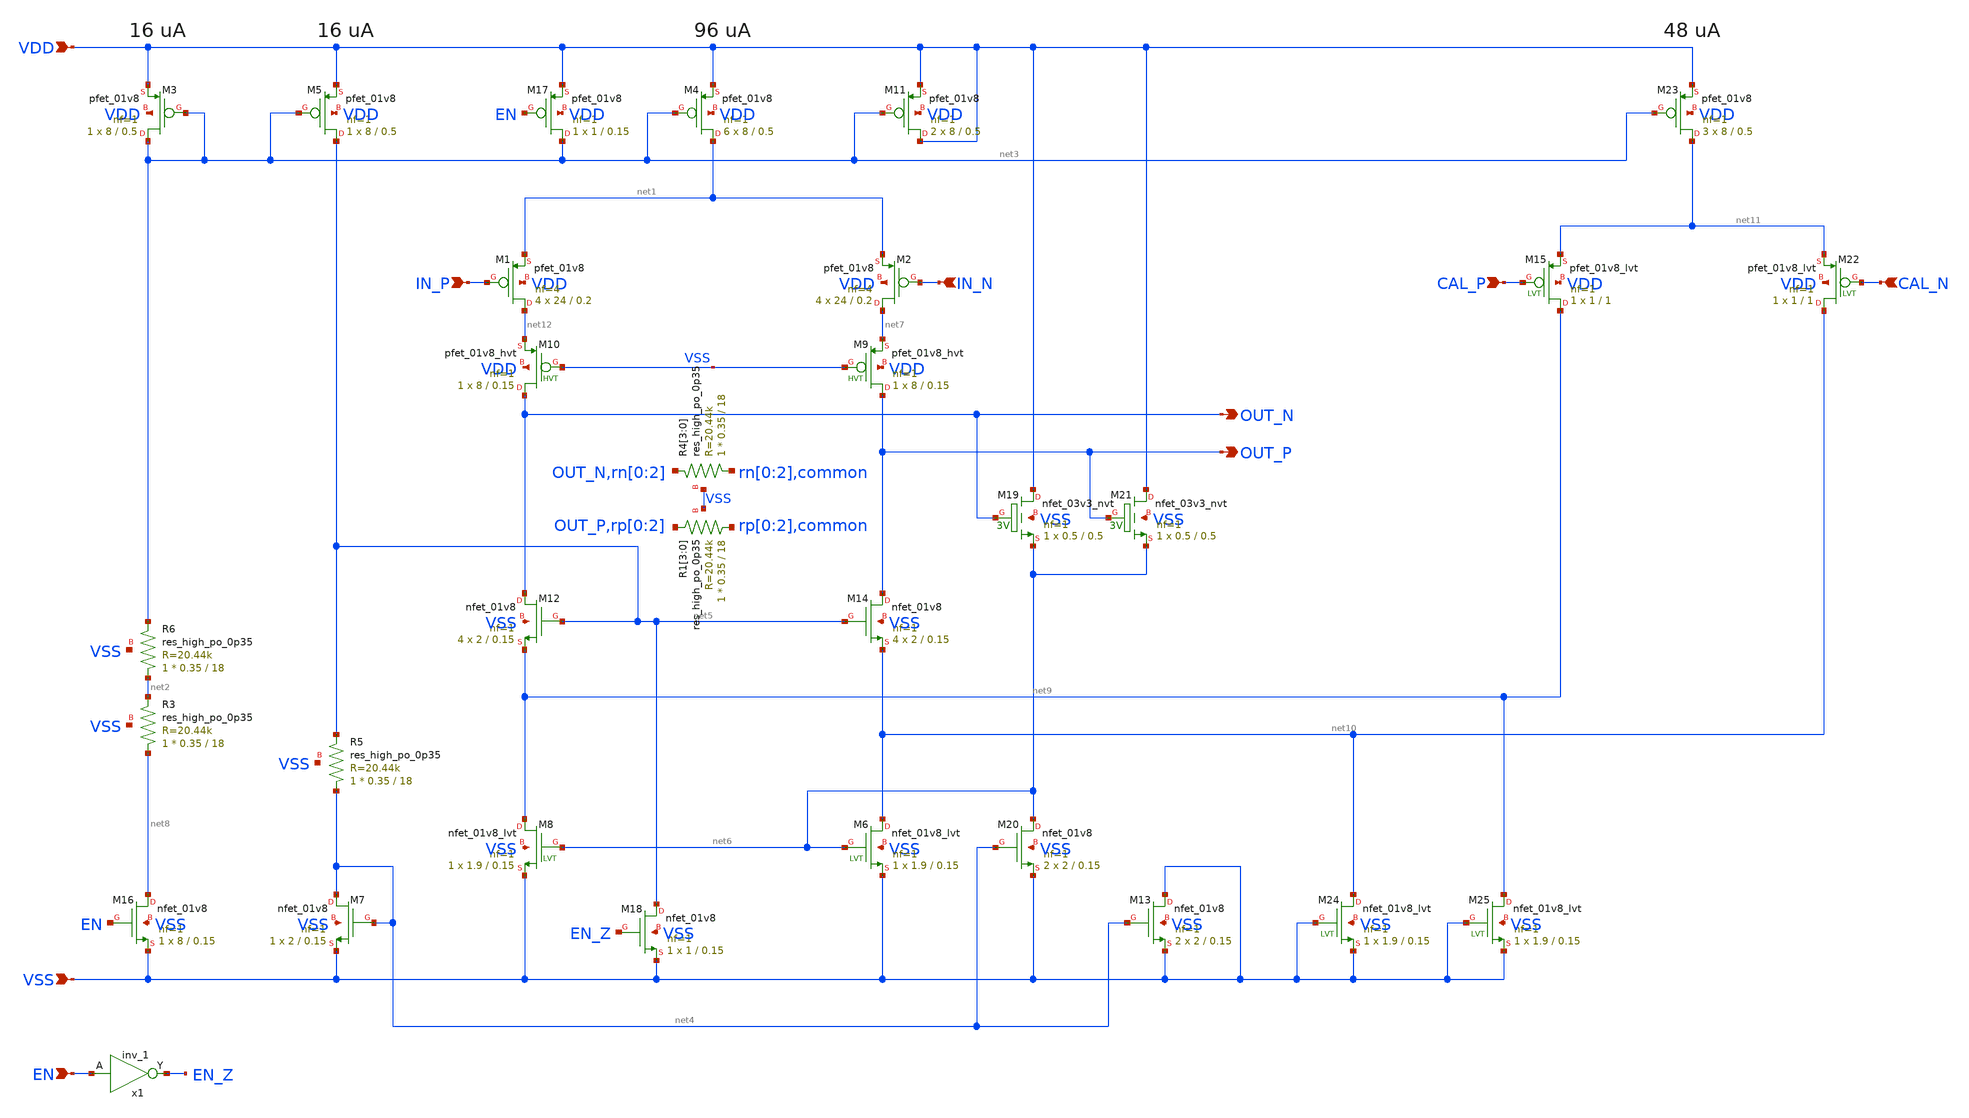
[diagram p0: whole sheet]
** sch_path: schematic/subcells/preamplifier/preamplifier.sch
**.subckt preamplifier VDD VSS IN_P IN_N OUT_P OUT_N EN CAL_P CAL_N
*.ipin VDD
*.ipin VSS
*.ipin IN_P
*.ipin IN_N
*.opin OUT_P
*.opin OUT_N
*.ipin EN
*.ipin CAL_P
*.ipin CAL_N
XM4 net1 net3 VDD VDD sky130_fd_pr__pfet_01v8 L=0.5 W=8 nf=1 ad='int((nf+1)/2) * W/nf * 0.29' as='int((nf+2)/2) * W/nf * 0.29'
+ pd='2*int((nf+1)/2) * (W/nf + 0.29)' ps='2*int((nf+2)/2) * (W/nf + 0.29)' nrd='0.29 / W' nrs='0.29 / W'
+ sa=0 sb=0 sd=0 mult=6 m=6
XM5 net5 net3 VDD VDD sky130_fd_pr__pfet_01v8 L=0.5 W=8 nf=1 ad='int((nf+1)/2) * W/nf * 0.29' as='int((nf+2)/2) * W/nf * 0.29'
+ pd='2*int((nf+1)/2) * (W/nf + 0.29)' ps='2*int((nf+2)/2) * (W/nf + 0.29)' nrd='0.29 / W' nrs='0.29 / W'
+ sa=0 sb=0 sd=0 mult=1 m=1
XM7 net4 net4 VSS VSS sky130_fd_pr__nfet_01v8 L=0.15 W=2 nf=1 ad='int((nf+1)/2) * W/nf * 0.29' as='int((nf+2)/2) * W/nf * 0.29'
+ pd='2*int((nf+1)/2) * (W/nf + 0.29)' ps='2*int((nf+2)/2) * (W/nf + 0.29)' nrd='0.29 / W' nrs='0.29 / W'
+ sa=0 sb=0 sd=0 mult=1 m=1
XM12 OUT_N net5 net9 VSS sky130_fd_pr__nfet_01v8 L=0.15 W=2 nf=1 ad='int((nf+1)/2) * W/nf * 0.29' as='int((nf+2)/2) * W/nf * 0.29'
+ pd='2*int((nf+1)/2) * (W/nf + 0.29)' ps='2*int((nf+2)/2) * (W/nf + 0.29)' nrd='0.29 / W' nrs='0.29 / W'
+ sa=0 sb=0 sd=0 mult=4 m=4
XM14 OUT_P net5 net10 VSS sky130_fd_pr__nfet_01v8 L=0.15 W=2 nf=1 ad='int((nf+1)/2) * W/nf * 0.29' as='int((nf+2)/2) * W/nf * 0.29'
+ pd='2*int((nf+1)/2) * (W/nf + 0.29)' ps='2*int((nf+2)/2) * (W/nf + 0.29)' nrd='0.29 / W' nrs='0.29 / W'
+ sa=0 sb=0 sd=0 mult=4 m=4
XM8 net9 net6 VSS VSS sky130_fd_pr__nfet_01v8_lvt L=0.15 W=1.9 nf=1 ad='int((nf+1)/2) * W/nf * 0.29'
+ as='int((nf+2)/2) * W/nf * 0.29' pd='2*int((nf+1)/2) * (W/nf + 0.29)' ps='2*int((nf+2)/2) * (W/nf + 0.29)'
+ nrd='0.29 / W' nrs='0.29 / W' sa=0 sb=0 sd=0 mult=1 m=1
XM6 net10 net6 VSS VSS sky130_fd_pr__nfet_01v8_lvt L=0.15 W=1.9 nf=1 ad='int((nf+1)/2) * W/nf * 0.29'
+ as='int((nf+2)/2) * W/nf * 0.29' pd='2*int((nf+1)/2) * (W/nf + 0.29)' ps='2*int((nf+2)/2) * (W/nf + 0.29)'
+ nrd='0.29 / W' nrs='0.29 / W' sa=0 sb=0 sd=0 mult=1 m=1
XM16 net8 EN VSS VSS sky130_fd_pr__nfet_01v8 L=0.15 W=8 nf=1 ad='int((nf+1)/2) * W/nf * 0.29' as='int((nf+2)/2) * W/nf * 0.29'
+ pd='2*int((nf+1)/2) * (W/nf + 0.29)' ps='2*int((nf+2)/2) * (W/nf + 0.29)' nrd='0.29 / W' nrs='0.29 / W'
+ sa=0 sb=0 sd=0 mult=1 m=1
XM17 net3 EN VDD VDD sky130_fd_pr__pfet_01v8 L=0.15 W=1 nf=1 ad='int((nf+1)/2) * W/nf * 0.29' as='int((nf+2)/2) * W/nf * 0.29'
+ pd='2*int((nf+1)/2) * (W/nf + 0.29)' ps='2*int((nf+2)/2) * (W/nf + 0.29)' nrd='0.29 / W' nrs='0.29 / W'
+ sa=0 sb=0 sd=0 mult=1 m=1
XM18 net5 EN_Z VSS VSS sky130_fd_pr__nfet_01v8 L=0.15 W=1 nf=1 ad='int((nf+1)/2) * W/nf * 0.29' as='int((nf+2)/2) * W/nf * 0.29'
+ pd='2*int((nf+1)/2) * (W/nf + 0.29)' ps='2*int((nf+2)/2) * (W/nf + 0.29)' nrd='0.29 / W' nrs='0.29 / W'
+ sa=0 sb=0 sd=0 mult=1 m=1
x1 EN VSS VSS VDD VDD EN_Z sky130_fd_sc_hd__inv_1
XM20 net6 net4 VSS VSS sky130_fd_pr__nfet_01v8 L=0.15 W=2 nf=1 ad='int((nf+1)/2) * W/nf * 0.29' as='int((nf+2)/2) * W/nf * 0.29'
+ pd='2*int((nf+1)/2) * (W/nf + 0.29)' ps='2*int((nf+2)/2) * (W/nf + 0.29)' nrd='0.29 / W' nrs='0.29 / W'
+ sa=0 sb=0 sd=0 mult=2 m=2
XM19 VDD OUT_N net6 VSS sky130_fd_pr__nfet_03v3_nvt L=0.5 W=0.5 nf=1 ad='int((nf+1)/2) * W/nf * 0.29'
+ as='int((nf+2)/2) * W/nf * 0.29' pd='2*int((nf+1)/2) * (W/nf + 0.29)' ps='2*int((nf+2)/2) * (W/nf + 0.29)'
+ nrd='0.29 / W' nrs='0.29 / W' sa=0 sb=0 sd=0 mult=1 m=1
XM21 VDD OUT_P net6 VSS sky130_fd_pr__nfet_03v3_nvt L=0.5 W=0.5 nf=1 ad='int((nf+1)/2) * W/nf * 0.29'
+ as='int((nf+2)/2) * W/nf * 0.29' pd='2*int((nf+1)/2) * (W/nf + 0.29)' ps='2*int((nf+2)/2) * (W/nf + 0.29)'
+ nrd='0.29 / W' nrs='0.29 / W' sa=0 sb=0 sd=0 mult=1 m=1
XM1 net12 IN_P net1 VDD sky130_fd_pr__pfet_01v8 L=0.2 W=24 nf=4 ad='int((nf+1)/2) * W/nf * 0.29' as='int((nf+2)/2) * W/nf * 0.29'
+ pd='2*int((nf+1)/2) * (W/nf + 0.29)' ps='2*int((nf+2)/2) * (W/nf + 0.29)' nrd='0.29 / W' nrs='0.29 / W'
+ sa=0 sb=0 sd=0 mult=4 m=4
XM2 net7 IN_N net1 VDD sky130_fd_pr__pfet_01v8 L=0.2 W=24 nf=4 ad='int((nf+1)/2) * W/nf * 0.29' as='int((nf+2)/2) * W/nf * 0.29'
+ pd='2*int((nf+1)/2) * (W/nf + 0.29)' ps='2*int((nf+2)/2) * (W/nf + 0.29)' nrd='0.29 / W' nrs='0.29 / W'
+ sa=0 sb=0 sd=0 mult=4 m=4
XM15 net9 CAL_P net11 VDD sky130_fd_pr__pfet_01v8_lvt L=1 W=1 nf=1 ad='int((nf+1)/2) * W/nf * 0.29' as='int((nf+2)/2) * W/nf * 0.29'
+ pd='2*int((nf+1)/2) * (W/nf + 0.29)' ps='2*int((nf+2)/2) * (W/nf + 0.29)' nrd='0.29 / W' nrs='0.29 / W'
+ sa=0 sb=0 sd=0 mult=1 m=1
XM22 net10 CAL_N net11 VDD sky130_fd_pr__pfet_01v8_lvt L=1 W=1 nf=1 ad='int((nf+1)/2) * W/nf * 0.29'
+ as='int((nf+2)/2) * W/nf * 0.29' pd='2*int((nf+1)/2) * (W/nf + 0.29)' ps='2*int((nf+2)/2) * (W/nf + 0.29)'
+ nrd='0.29 / W' nrs='0.29 / W' sa=0 sb=0 sd=0 mult=1 m=1
XM3 net3 net3 VDD VDD sky130_fd_pr__pfet_01v8 L=0.5 W=8 nf=1 ad='int((nf+1)/2) * W/nf * 0.29' as='int((nf+2)/2) * W/nf * 0.29'
+ pd='2*int((nf+1)/2) * (W/nf + 0.29)' ps='2*int((nf+2)/2) * (W/nf + 0.29)' nrd='0.29 / W' nrs='0.29 / W'
+ sa=0 sb=0 sd=0 mult=1 m=1
XR6 net2 net3 VSS sky130_fd_pr__res_high_po_0p35 L=18 mult=1 m=1
XM23 net11 net3 VDD VDD sky130_fd_pr__pfet_01v8 L=0.5 W=8 nf=1 ad='int((nf+1)/2) * W/nf * 0.29' as='int((nf+2)/2) * W/nf * 0.29'
+ pd='2*int((nf+1)/2) * (W/nf + 0.29)' ps='2*int((nf+2)/2) * (W/nf + 0.29)' nrd='0.29 / W' nrs='0.29 / W'
+ sa=0 sb=0 sd=0 mult=3 m=3
XR3 net8 net2 VSS sky130_fd_pr__res_high_po_0p35 L=18 mult=1 m=1
XR4[3] rn[0] OUT_N VSS sky130_fd_pr__res_high_po_0p35 L=18 mult=1 m=1
XR4[2] rn[1] rn[0] VSS sky130_fd_pr__res_high_po_0p35 L=18 mult=1 m=1
XR4[1] rn[2] rn[1] VSS sky130_fd_pr__res_high_po_0p35 L=18 mult=1 m=1
XR4[0] common rn[2] VSS sky130_fd_pr__res_high_po_0p35 L=18 mult=1 m=1
XR5 net4 net5 VSS sky130_fd_pr__res_high_po_0p35 L=18 mult=1 m=1
XM9 OUT_P VSS net7 VDD sky130_fd_pr__pfet_01v8_hvt L=0.15 W=8 nf=1 ad='int((nf+1)/2) * W/nf * 0.29' as='int((nf+2)/2) * W/nf * 0.29'
+ pd='2*int((nf+1)/2) * (W/nf + 0.29)' ps='2*int((nf+2)/2) * (W/nf + 0.29)' nrd='0.29 / W' nrs='0.29 / W'
+ sa=0 sb=0 sd=0 mult=1 m=1
XM10 OUT_N VSS net12 VDD sky130_fd_pr__pfet_01v8_hvt L=0.15 W=8 nf=1 ad='int((nf+1)/2) * W/nf * 0.29'
+ as='int((nf+2)/2) * W/nf * 0.29' pd='2*int((nf+1)/2) * (W/nf + 0.29)' ps='2*int((nf+2)/2) * (W/nf + 0.29)'
+ nrd='0.29 / W' nrs='0.29 / W' sa=0 sb=0 sd=0 mult=1 m=1
XR1[3] rp[0] OUT_P VSS sky130_fd_pr__res_high_po_0p35 L=18 mult=1 m=1
XR1[2] rp[1] rp[0] VSS sky130_fd_pr__res_high_po_0p35 L=18 mult=1 m=1
XR1[1] rp[2] rp[1] VSS sky130_fd_pr__res_high_po_0p35 L=18 mult=1 m=1
XR1[0] common rp[2] VSS sky130_fd_pr__res_high_po_0p35 L=18 mult=1 m=1
XM11 VDD net3 VDD VDD sky130_fd_pr__pfet_01v8 L=0.5 W=8 nf=1 ad='int((nf+1)/2) * W/nf * 0.29' as='int((nf+2)/2) * W/nf * 0.29'
+ pd='2*int((nf+1)/2) * (W/nf + 0.29)' ps='2*int((nf+2)/2) * (W/nf + 0.29)' nrd='0.29 / W' nrs='0.29 / W'
+ sa=0 sb=0 sd=0 mult=2 m=2
XM13 VSS net4 VSS VSS sky130_fd_pr__nfet_01v8 L=0.15 W=2 nf=1 ad='int((nf+1)/2) * W/nf * 0.29' as='int((nf+2)/2) * W/nf * 0.29'
+ pd='2*int((nf+1)/2) * (W/nf + 0.29)' ps='2*int((nf+2)/2) * (W/nf + 0.29)' nrd='0.29 / W' nrs='0.29 / W'
+ sa=0 sb=0 sd=0 mult=2 m=2
XM24 net10 VSS VSS VSS sky130_fd_pr__nfet_01v8_lvt L=0.15 W=1.9 nf=1 ad='int((nf+1)/2) * W/nf * 0.29'
+ as='int((nf+2)/2) * W/nf * 0.29' pd='2*int((nf+1)/2) * (W/nf + 0.29)' ps='2*int((nf+2)/2) * (W/nf + 0.29)'
+ nrd='0.29 / W' nrs='0.29 / W' sa=0 sb=0 sd=0 mult=1 m=1
XM25 net9 VSS VSS VSS sky130_fd_pr__nfet_01v8_lvt L=0.15 W=1.9 nf=1 ad='int((nf+1)/2) * W/nf * 0.29'
+ as='int((nf+2)/2) * W/nf * 0.29' pd='2*int((nf+1)/2) * (W/nf + 0.29)' ps='2*int((nf+2)/2) * (W/nf + 0.29)'
+ nrd='0.29 / W' nrs='0.29 / W' sa=0 sb=0 sd=0 mult=1 m=1
**.ends
.end
